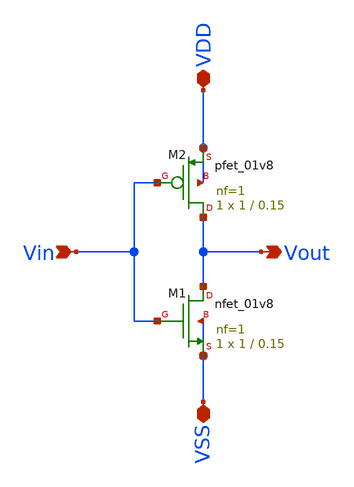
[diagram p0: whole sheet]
** sch_path: xschem/vco_inverter.sch
**.subckt vco_inverter VDD VSS Vin Vout
*.iopin VDD
*.iopin VSS
*.ipin Vin
*.opin Vout
XM1 Vout Vin VSS VSS sky130_fd_pr__nfet_01v8 L=0.15 W=1 nf=1 ad='int((nf+1)/2) * W/nf * 0.29' as='int((nf+2)/2) * W/nf * 0.29'
+ pd='2*int((nf+1)/2) * (W/nf + 0.29)' ps='2*int((nf+2)/2) * (W/nf + 0.29)' nrd='0.29 / W' nrs='0.29 / W'
+ sa=0 sb=0 sd=0 mult=1 m=1
XM2 Vout Vin VDD VDD sky130_fd_pr__pfet_01v8 L=0.15 W=1 nf=1 ad='int((nf+1)/2) * W/nf * 0.29' as='int((nf+2)/2) * W/nf * 0.29'
+ pd='2*int((nf+1)/2) * (W/nf + 0.29)' ps='2*int((nf+2)/2) * (W/nf + 0.29)' nrd='0.29 / W' nrs='0.29 / W'
+ sa=0 sb=0 sd=0 mult=1 m=1
**.ends
.end
